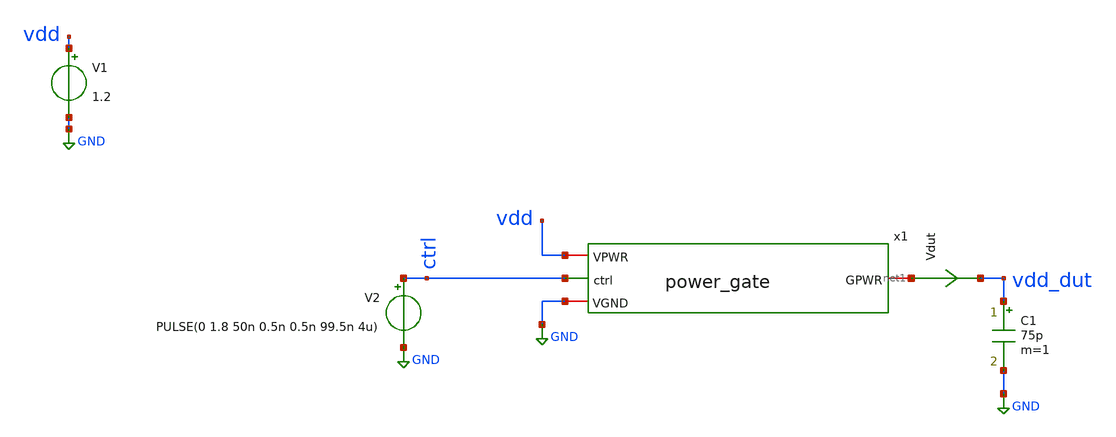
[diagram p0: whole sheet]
** sch_path: ihp-sg13cmos5l/libs.tech/xschem/tests/tb_power_gate.sch
**.subckt tb_power_gate
x1 vdd net1 ctrl GND power_gate
V1 vdd GND 1.2
.save i(v1)
V2 ctrl GND PULSE(0 1.8 50n 0.5n 0.5n 99.5n 4u)
C1 vdd_dut GND 75p m=1
Vdut net1 vdd_dut 0
.save i(vdut)
**** begin user architecture code

.lib cornerMOSlv.lib mos_tt
*.lib cornerCAP.lib cap_typ



.param mc_mm_switch=0
.control
save all
tran 50p 5u
plot vdd_dut
plot vdd_dut x1.ctrl_n ctrl xlimit 50n 60n
*quit 0
.endc
.end


**** end user architecture code
**.ends

* expanding   symbol:
*+  /home/designer/shared/hm-openpdk-library/ihp-sg13cmos5l/libs.tech/xschem/hm_analog/power_gate.sym # of pins=4
** sym_path: ihp-sg13cmos5l/libs.tech/xschem/hm_analog/power_gate.sym
** sch_path: ihp-sg13cmos5l/libs.tech/xschem/hm_analog/power_gate.sch
.subckt power_gate VPWR GPWR ctrl VGND
*.ipin ctrl
*.iopin VPWR
*.iopin VGND
*.iopin GPWR
XM1 ctrl_n ctrl VGND VGND sg13_lv_nmos w=2.6u l=0.13u ng=1 m=1 mm_ok=1
XM2 ctrl_n ctrl VPWR VPWR sg13_lv_pmos w=4.44u l=0.13u ng=1 m=1 mm_ok=1
XM3 GPWR ctrl_n VPWR VPWR sg13_lv_pmos w=2175u l=0.13u ng=290 m=1 mm_ok=1
x1 VGND GPWR ctrl_n dischg
.ends


* expanding   symbol:
*+  /home/designer/shared/hm-openpdk-library/ihp-sg13cmos5l/libs.tech/xschem/hm_analog/dischg.sym # of pins=3
** sym_path: ihp-sg13cmos5l/libs.tech/xschem/hm_analog/dischg.sym
** sch_path: ihp-sg13cmos5l/libs.tech/xschem/hm_analog/dischg.sch
.subckt dischg VGND GPWR gate
*.iopin GPWR
*.iopin VGND
*.ipin gate
XM1 GPWR gate net6 GPWR sg13_lv_nmos w=0.50u l=0.65u ng=1 m=1 mm_ok=1
XM2 net6 gate net5 net6 sg13_lv_nmos w=0.50u l=0.65u ng=1 m=1 mm_ok=1
XM3 net5 gate net4 net5 sg13_lv_nmos w=0.50u l=0.65u ng=1 m=1 mm_ok=1
XM4 net4 gate VGND net4 sg13_lv_nmos w=0.50u l=0.65u ng=1 m=1 mm_ok=1
XM5 GPWR gate net3 GPWR sg13_lv_nmos w=0.50u l=0.65u ng=1 m=1 mm_ok=1
XM6 net3 gate net2 net3 sg13_lv_nmos w=0.50u l=0.65u ng=1 m=1 mm_ok=1
XM7 net2 gate net1 net2 sg13_lv_nmos w=0.50u l=0.65u ng=1 m=1 mm_ok=1
XM8 net1 gate VGND net1 sg13_lv_nmos w=0.50u l=0.65u ng=1 m=1 mm_ok=1
.ends

.GLOBAL GND
.end
